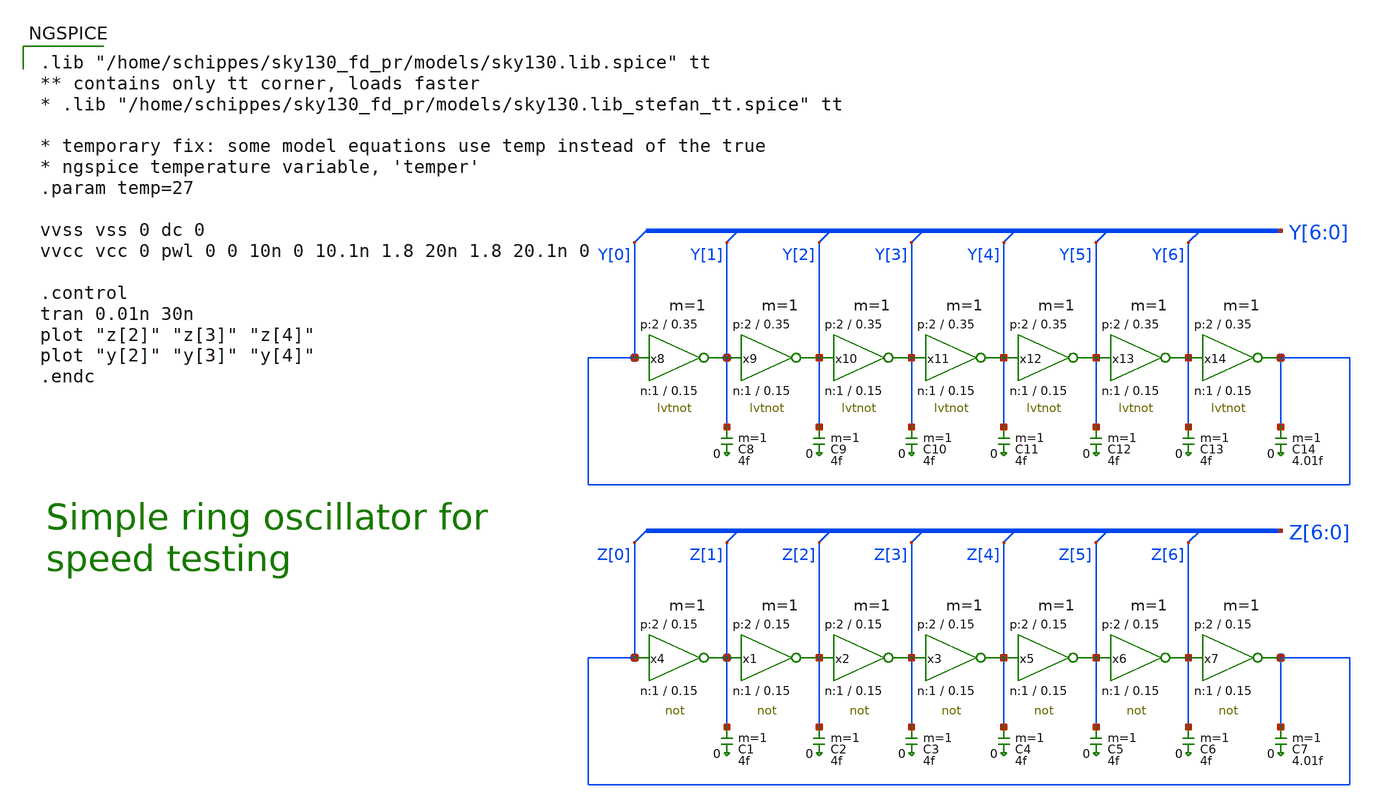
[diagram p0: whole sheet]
** sch_path: sky130_tests/test_inv.sch
**.subckt test_inv
x4 Z[1] Z[0] VCC VSS not W_N=1 L_N=0.15 W_P=2 L_P=0.15 m=1
C1 Z[1] 0 4f m=1
x1 Z[2] Z[1] VCC VSS not W_N=1 L_N=0.15 W_P=2 L_P=0.15 m=1
x2 Z[3] Z[2] VCC VSS not W_N=1 L_N=0.15 W_P=2 L_P=0.15 m=1
x3 Z[4] Z[3] VCC VSS not W_N=1 L_N=0.15 W_P=2 L_P=0.15 m=1
x5 Z[5] Z[4] VCC VSS not W_N=1 L_N=0.15 W_P=2 L_P=0.15 m=1
x6 Z[6] Z[5] VCC VSS not W_N=1 L_N=0.15 W_P=2 L_P=0.15 m=1
x7 Z[0] Z[6] VCC VSS not W_N=1 L_N=0.15 W_P=2 L_P=0.15 m=1
C2 Z[2] 0 4f m=1
C3 Z[3] 0 4f m=1
C4 Z[4] 0 4f m=1
C5 Z[5] 0 4f m=1
C6 Z[6] 0 4f m=1
C7 Z[0] 0 4.01f m=1
x8 Y[1] Y[0] VCC VSS lvtnot W_N=1 L_N=0.15 W_P=2 L_P=0.35 m=1
C8 Y[1] 0 4f m=1
x9 Y[2] Y[1] VCC VSS lvtnot W_N=1 L_N=0.15 W_P=2 L_P=0.35 m=1
x10 Y[3] Y[2] VCC VSS lvtnot W_N=1 L_N=0.15 W_P=2 L_P=0.35 m=1
x11 Y[4] Y[3] VCC VSS lvtnot W_N=1 L_N=0.15 W_P=2 L_P=0.35 m=1
x12 Y[5] Y[4] VCC VSS lvtnot W_N=1 L_N=0.15 W_P=2 L_P=0.35 m=1
x13 Y[6] Y[5] VCC VSS lvtnot W_N=1 L_N=0.15 W_P=2 L_P=0.35 m=1
x14 Y[0] Y[6] VCC VSS lvtnot W_N=1 L_N=0.15 W_P=2 L_P=0.35 m=1
C9 Y[2] 0 4f m=1
C10 Y[3] 0 4f m=1
C11 Y[4] 0 4f m=1
C12 Y[5] 0 4f m=1
C13 Y[6] 0 4f m=1
C14 Y[0] 0 4.01f m=1
**** begin user architecture code

.lib "/home/schippes/sky130_fd_pr/models/sky130.lib.spice" tt
** contains only tt corner, loads faster
* .lib "/home/schippes/sky130_fd_pr/models/sky130.lib_stefan_tt.spice" tt

* temporary fix: some model equations use temp instead of the true
* ngspice temperature variable, 'temper'
.param temp=27

vvss vss 0 dc 0
vvcc vcc 0 pwl 0 0 10n 0 10.1n 1.8 20n 1.8 20.1n 0

.control
tran 0.01n 30n
plot "z[2]" "z[3]" "z[4]"
plot "y[2]" "y[3]" "y[4]"
.endc


**** end user architecture code
**.ends

* expanding   symbol:  sky130_tests/not.sym # of pins=2
** sym_path: sky130_tests/not.sym
** sch_path: sky130_tests/not.sch
.subckt not y a VCCPIN VSSPIN     W_N=1 L_N=0.15 W_P=2 L_P=0.15
*.opin y
*.ipin a
XM1 y a VSSPIN VSSPIN sky130_fd_pr__nfet_01v8 W=W_N L=L_N ad='W * 0.29' pd='W + 2 * 0.29' as='W * 0.29'
+ ps='W + 2 * 0.29' nrd=0 nrs=0 sa=0 sb=0 sd=0 nf=1 mult=1
XM2 y a VCCPIN VCCPIN sky130_fd_pr__pfet_01v8 W=W_P L=L_P ad='W * 0.29' pd='W + 2 * 0.29' as='W * 0.29'
+ ps='W + 2 * 0.29' nrd=0 nrs=0 sa=0 sb=0 sd=0 nf=1 mult=1
.ends


* expanding   symbol:  sky130_tests/lvtnot.sym # of pins=2
** sym_path: sky130_tests/lvtnot.sym
** sch_path: sky130_tests/lvtnot.sch
.subckt lvtnot y a VCCPIN VSSPIN     W_N=1 L_N=0.15 W_P=2 L_P=0.35
*.opin y
*.ipin a
XM1 y a VSSPIN VSSPIN sky130_fd_pr__nfet_01v8_lvt W=W_N L=L_N ad='W * 0.29' pd='W + 2 * 0.29' as='W * 0.29'
+ ps='W + 2 * 0.29' nrd=0 nrs=0 sa=0 sb=0 sd=0 nf=1 mult=1
XM2 y a VCCPIN VCCPIN sky130_fd_pr__pfet_01v8_lvt W=W_P L=L_P ad='W * 0.29' pd='W + 2 * 0.29' as='W * 0.29'
+ ps='W + 2 * 0.29' nrd=0 nrs=0 sa=0 sb=0 sd=0 nf=1 mult=1
.ends

.end
